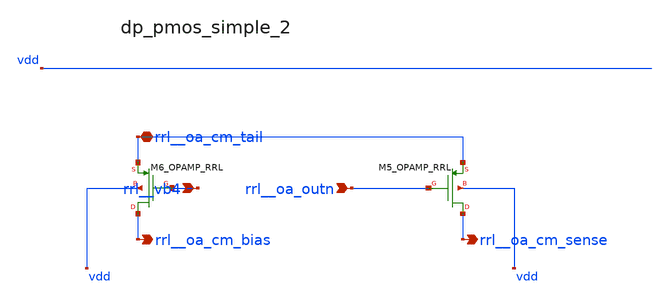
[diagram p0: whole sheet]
** sch_path: analog-db/raw/ia_004_fan_chopper_rrl/hier/blocks/dp_pmos_simple_2.sch
**.subckt dp_pmos_simple_2 rrl__vb4 rrl__oa_outn rrl__oa_cm_tail rrl__oa_cm_bias rrl__oa_cm_sense
*.ipin rrl__vb4
*.ipin rrl__oa_outn
*.iopin rrl__oa_cm_tail
*.opin rrl__oa_cm_bias
*.opin rrl__oa_cm_sense
XM5_OPAMP_RRL rrl__oa_cm_sense rrl__oa_outn rrl__oa_cm_tail vdd sg13_lv_pmos w=x_dut_xm5_opamp_rrl_w
+ l=x_dut_xm5_opamp_rrl_l ng=1 m=x_dut_xm5_opamp_rrl_m
XM6_OPAMP_RRL rrl__oa_cm_bias rrl__vb4 rrl__oa_cm_tail vdd sg13_lv_pmos w=x_dut_xm6_opamp_rrl_w
+ l=x_dut_xm6_opamp_rrl_l ng=1 m=x_dut_xm6_opamp_rrl_m
**.ends
.end
